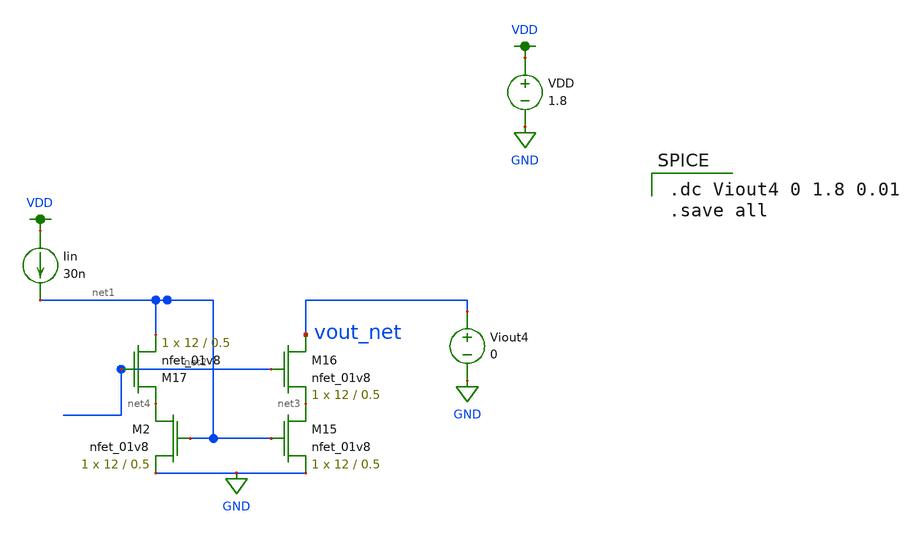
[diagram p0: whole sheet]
** sch_path: schematics/current mirrors/folded_cascode_current_mirror_2.sch
**.subckt folded_cascode_current_mirror_2
VDD VDD GND 1.8
XM15 net3 net1 GND GND sky130_fd_pr__nfet_01v8 L=0.5 W=12 nf=1 ad='int((nf+1)/2) * W/nf * 0.29' as='int((nf+2)/2) * W/nf * 0.29'
+ pd='2*int((nf+1)/2) * (W/nf + 0.29)' ps='2*int((nf+2)/2) * (W/nf + 0.29)' nrd='0.29 / W' nrs='0.29 / W'
+ sa=0 sb=0 sd=0 mult=1 m=1
XM16 vout_net net2 net3 GND sky130_fd_pr__nfet_01v8 L=0.5 W=12 nf=1 ad='int((nf+1)/2) * W/nf * 0.29'
+ as='int((nf+2)/2) * W/nf * 0.29' pd='2*int((nf+1)/2) * (W/nf + 0.29)' ps='2*int((nf+2)/2) * (W/nf + 0.29)'
+ nrd='0.29 / W' nrs='0.29 / W' sa=0 sb=0 sd=0 mult=1 m=1
XM2 net4 net1 GND GND sky130_fd_pr__nfet_01v8 L=0.5 W=12 nf=1 ad='int((nf+1)/2) * W/nf * 0.29' as='int((nf+2)/2) * W/nf * 0.29'
+ pd='2*int((nf+1)/2) * (W/nf + 0.29)' ps='2*int((nf+2)/2) * (W/nf + 0.29)' nrd='0.29 / W' nrs='0.29 / W'
+ sa=0 sb=0 sd=0 mult=1 m=1
XM17 net4 net2 net1 GND sky130_fd_pr__nfet_01v8 L=0.5 W=12 nf=1 ad='int((nf+1)/2) * W/nf * 0.29' as='int((nf+2)/2) * W/nf * 0.29'
+ pd='2*int((nf+1)/2) * (W/nf + 0.29)' ps='2*int((nf+2)/2) * (W/nf + 0.29)' nrd='0.29 / W' nrs='0.29 / W'
+ sa=0 sb=0 sd=0 mult=1 m=1
Iin VDD net1 30n
Viout4 vout_net GND 0
**** begin user architecture code

.option wnflag=1
.param MC_SWITCH=0.0
.lib ~/skywater/skywater-pdk/libraries/sky130_fd_pr_ngspice/latest/models/sky130.lib.spice tt


.dc Viout4 0 1.8 0.01
.save all

**** end user architecture code
**.ends
.GLOBAL VDD
.GLOBAL GND
.end
